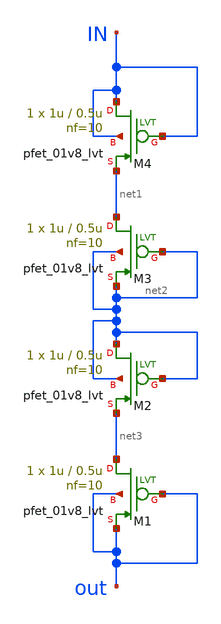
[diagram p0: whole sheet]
** sch_path: pseudoresistor.sch
**.subckt pseudoresistor
XM1 net3 out out out sky130_fd_pr__pfet_01v8_lvt L=0.5u W=1u nf=10 ad='int((nf+1)/2) * W/nf * 0.29' as='int((nf+2)/2) * W/nf * 0.29'
+ pd='2*int((nf+1)/2) * (W/nf + 0.29)' ps='2*int((nf+2)/2) * (W/nf + 0.29)' nrd='0.29 / W' nrs='0.29 / W'
+ sa=0 sb=0 sd=0 mult=1 m=1
XM2 net2 net2 net3 net2 sky130_fd_pr__pfet_01v8_lvt L=0.5u W=1u nf=10 ad='int((nf+1)/2) * W/nf * 0.29'
+ as='int((nf+2)/2) * W/nf * 0.29' pd='2*int((nf+1)/2) * (W/nf + 0.29)' ps='2*int((nf+2)/2) * (W/nf + 0.29)'
+ nrd='0.29 / W' nrs='0.29 / W' sa=0 sb=0 sd=0 mult=1 m=1
XM3 net1 net2 net2 net2 sky130_fd_pr__pfet_01v8_lvt L=0.5u W=1u nf=10 ad='int((nf+1)/2) * W/nf * 0.29'
+ as='int((nf+2)/2) * W/nf * 0.29' pd='2*int((nf+1)/2) * (W/nf + 0.29)' ps='2*int((nf+2)/2) * (W/nf + 0.29)'
+ nrd='0.29 / W' nrs='0.29 / W' sa=0 sb=0 sd=0 mult=1 m=1
XM4 IN IN net1 IN sky130_fd_pr__pfet_01v8_lvt L=0.5u W=1u nf=10 ad='int((nf+1)/2) * W/nf * 0.29' as='int((nf+2)/2) * W/nf * 0.29'
+ pd='2*int((nf+1)/2) * (W/nf + 0.29)' ps='2*int((nf+2)/2) * (W/nf + 0.29)' nrd='0.29 / W' nrs='0.29 / W'
+ sa=0 sb=0 sd=0 mult=1 m=1
**.ends
.end
